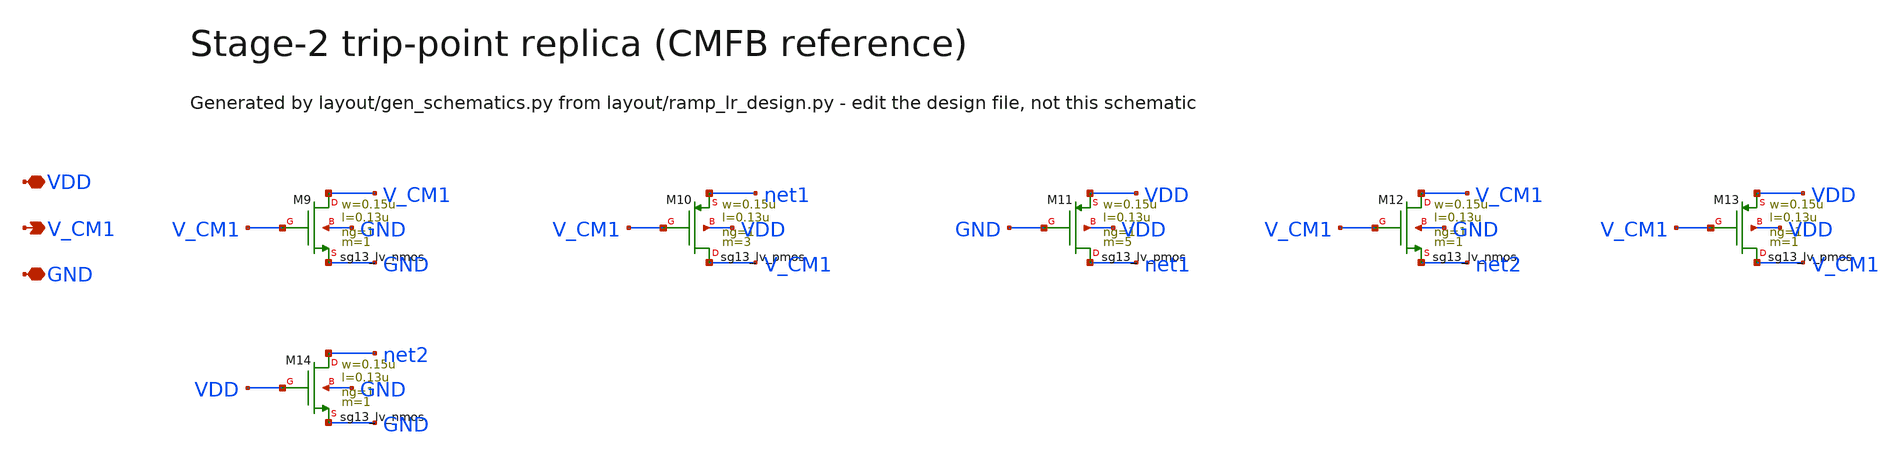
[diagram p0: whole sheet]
** sch_path: Design Files/RAMP/RAMP-LR/STG1_CM_LR.sch
**.subckt STG1_CM_LR VDD V_CM1 GND
*.iopin VDD
*.opin V_CM1
*.iopin GND
XM9 V_CM1 V_CM1 GND GND sg13_lv_nmos w=0.15u l=0.13u ng=1 m=1 mm_ok=1
XM10 V_CM1 V_CM1 net1 VDD sg13_lv_pmos w=0.15u l=0.13u ng=1 m=3 mm_ok=1
XM11 net1 GND VDD VDD sg13_lv_pmos w=0.15u l=0.13u ng=1 m=5 mm_ok=1
XM12 V_CM1 V_CM1 net2 GND sg13_lv_nmos w=0.15u l=0.13u ng=1 m=1 mm_ok=1
XM13 V_CM1 V_CM1 VDD VDD sg13_lv_pmos w=0.15u l=0.13u ng=1 m=1 mm_ok=1
XM14 net2 VDD GND GND sg13_lv_nmos w=0.15u l=0.13u ng=1 m=1 mm_ok=1
**.ends
.end
